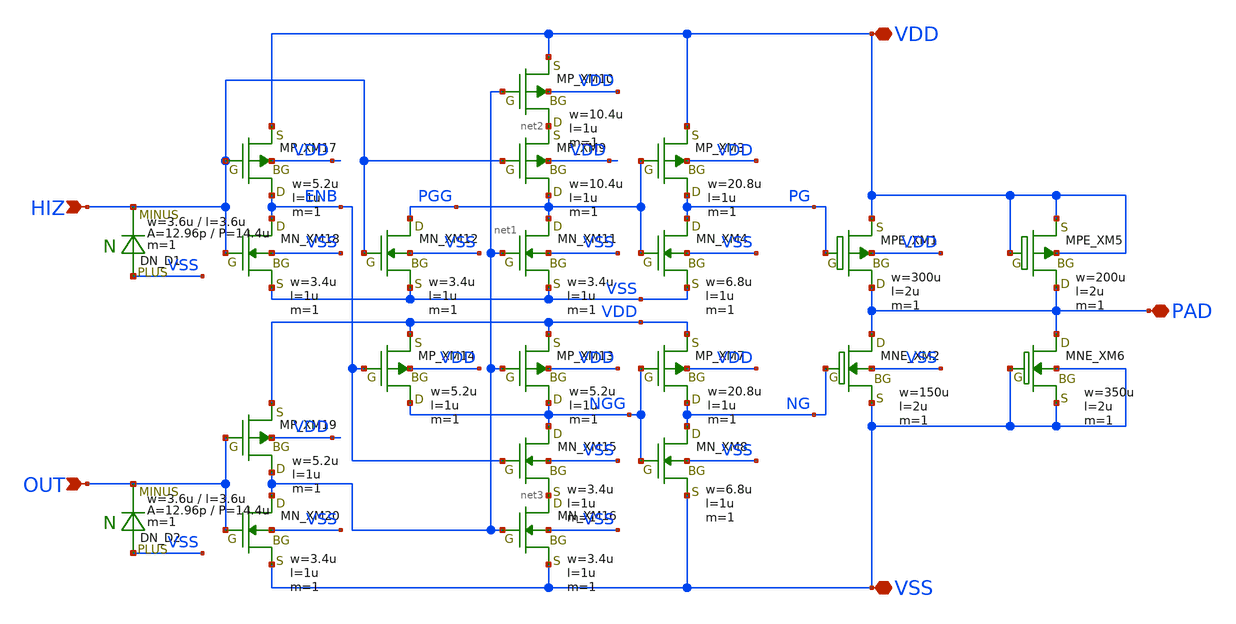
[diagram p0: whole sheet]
** sch_path: libs.tech/xschem/TR-1um_frame/OSS_ESD_5V_DIO.sch
**.subckt OSS_ESD_5V_DIO PAD VDD VSS HIZ OUT
*.iopin PAD
*.iopin VDD
*.iopin VSS
*.ipin HIZ
*.ipin OUT
XXM1 PAD PG VDD VDD MPE w=300u l=2u as=0 ad=0 ps=0 pd=0 nrd=0 nrs=0 m=1
XXM2 PAD NG VSS VSS MNE w=150u l=2u as=0 ad=0 ps=0 pd=0 nrd=0 nrs=0 m=1
XXM3 PG PGG VDD VDD PMOS w=20.8u l=1u nrd=0 nrs=0 m=1
XXM4 PG PGG VSS VSS NMOS w=6.8u l=1u nrd=0 nrs=0 m=1
XXM5 PAD VDD VDD VDD MPE w=200u l=2u as=0 ad=0 ps=0 pd=0 nrd=0 nrs=0 m=1
XXM6 PAD VSS VSS VSS MNE w=350u l=2u as=0 ad=0 ps=0 pd=0 nrd=0 nrs=0 m=1
XXM7 NG NGG VDD VDD PMOS w=20.8u l=1u nrd=0 nrs=0 m=1
XXM8 NG NGG VSS VSS NMOS w=6.8u l=1u nrd=0 nrs=0 m=1
XXM9 PGG HIZ net2 VDD PMOS w=10.4u l=1u nrd=0 nrs=0 m=1
XXM10 net2 net1 VDD VDD PMOS w=10.4u l=1u nrd=0 nrs=0 m=1
XXM11 PGG net1 VSS VSS NMOS w=3.4u l=1u nrd=0 nrs=0 m=1
XXM12 PGG HIZ VSS VSS NMOS w=3.4u l=1u nrd=0 nrs=0 m=1
XXM13 NGG net1 VDD VDD PMOS w=5.2u l=1u nrd=0 nrs=0 m=1
XXM14 NGG ENB VDD VDD PMOS w=5.2u l=1u nrd=0 nrs=0 m=1
XXM15 NGG ENB net3 VSS NMOS w=3.4u l=1u nrd=0 nrs=0 m=1
XXM16 net3 net1 VSS VSS NMOS w=3.4u l=1u nrd=0 nrs=0 m=1
XXM17 ENB HIZ VDD VDD PMOS w=5.2u l=1u nrd=0 nrs=0 m=1
XXM18 ENB HIZ VSS VSS NMOS w=3.4u l=1u nrd=0 nrs=0 m=1
DD1 VSS HIZ DN m=1
XXM19 net1 OUT VDD VDD PMOS w=5.2u l=1u nrd=0 nrs=0 m=1
XXM20 net1 OUT VSS VSS NMOS w=3.4u l=1u nrd=0 nrs=0 m=1
DD2 VSS OUT DN m=1
**.ends
.end
